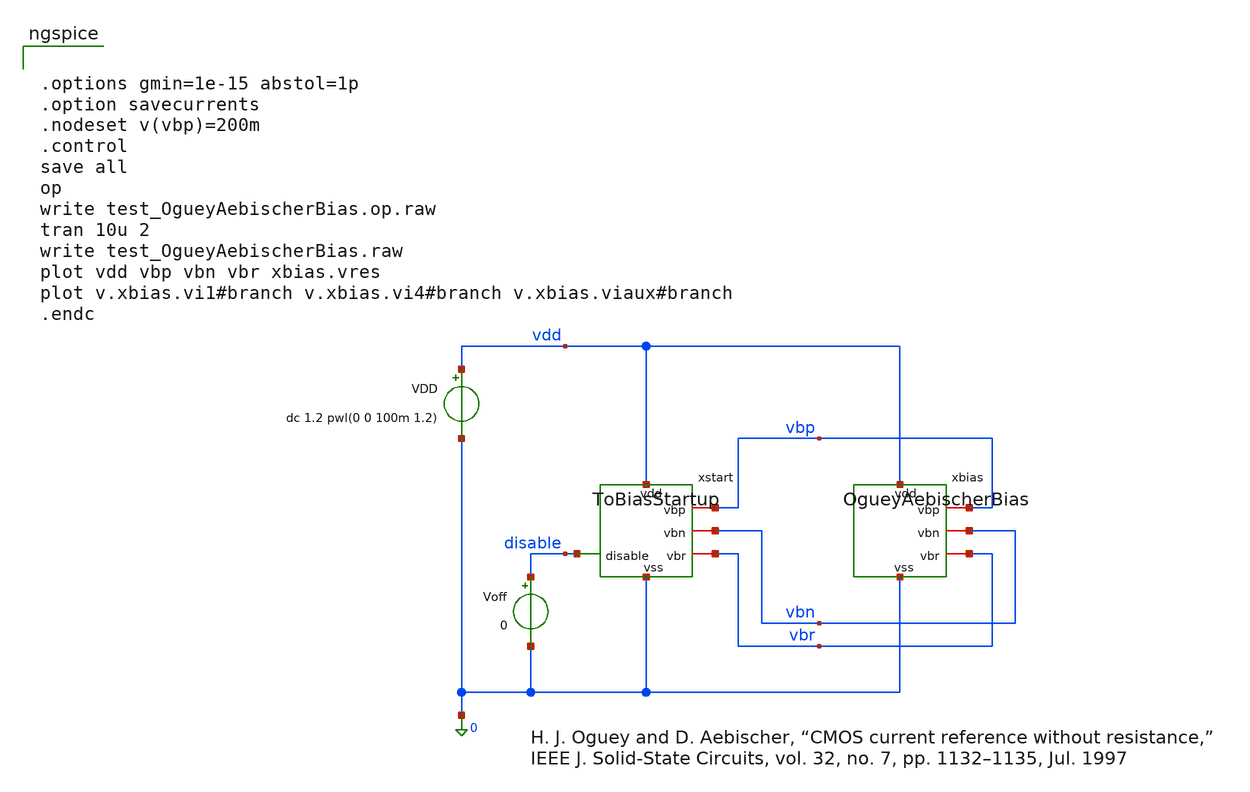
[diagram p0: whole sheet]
** sch_path: playground/test_OgueyAebischerBias.sch
**.subckt test_OgueyAebischerBias
xbias vdd vbp vbn vbr 0 OgueyAebischerBias
xstart vdd vbp vbn disable vbr 0 ToBiasStartup
VDD vdd 0 dc 1.2 pwl(0 0 100m 1.2)
Voff disable 0 0
**** begin user architecture code


.options gmin=1e-15 abstol=1p
.option savecurrents
.nodeset v(vbp)=200m
.control
save all
op
write test_OgueyAebischerBias.op.raw
tran 10u 2
write test_OgueyAebischerBias.raw
plot vdd vbp vbn vbr xbias.vres
plot v.xbias.vi1#branch v.xbias.vi4#branch v.xbias.viaux#branch
.endc


 .lib $::SKYWATER_MODELS/models/sky130.lib.spice tt

.param mc_mm_switch=0
.param mc_pr_switch=1


**** end user architecture code
**.ends

* expanding   symbol:  OgueyAebischerBias.sym # of pins=5
** sym_path: OgueyAebischerBias.sym
** sch_path: OgueyAebischerBias.sch
.subckt OgueyAebischerBias vdd vbp vbn vbr vss
*.iopin vss
*.iopin vdd
*.iopin vbp
*.iopin vbn
*.iopin vbr
XM10 net3 vbn vres vss sky130_fd_pr__nfet_01v8 L=1 W=1 nf=1 ad='int((1 + 1)/2) * 1 / 1 * 0.29' as='int((1 + 2)/2) * 1 / 1 * 0.29'
+ pd='2*int((1 + 1)/2) * (1 / 1 + 0.29)' ps='2*int((1 + 2)/2) * (1 / 1 + 0.29)' nrd='0.29 / 1 ' nrs='0.29 / 1 '
+ sa=0 sb=0 sd=0 mult=4 m=4
XM12 vbp vbp vdd vdd sky130_fd_pr__pfet_01v8 L=1 W=1 nf=1 ad='int((nf+1)/2) * W/nf * 0.29' as='int((nf+2)/2) * W/nf * 0.29'
+ pd='2*int((nf+1)/2) * (W/nf + 0.29)' ps='2*int((nf+2)/2) * (W/nf + 0.29)' nrd='0.29 / W' nrs='0.29 / W'
+ sa=0 sb=0 sd=0 mult=1 m=1
XM11 vbn vbn vss vss sky130_fd_pr__nfet_01v8 L=1 W=1 nf=1 ad='int((1 + 1)/2) * 1 / 1 * 0.29' as='int((1 + 2)/2) * 1 / 1 * 0.29'
+ pd='2*int((1 + 1)/2) * (1 / 1 + 0.29)' ps='2*int((1 + 2)/2) * (1 / 1 + 0.29)' nrd='0.29 / 1 ' nrs='0.29 / 1 '
+ sa=0 sb=0 sd=0 mult=1 m=1
XM13 net2 vbp vdd vdd sky130_fd_pr__pfet_01v8 L=1 W=1 nf=1 ad='int((nf+1)/2) * W/nf * 0.29' as='int((nf+2)/2) * W/nf * 0.29'
+ pd='2*int((nf+1)/2) * (W/nf + 0.29)' ps='2*int((nf+2)/2) * (W/nf + 0.29)' nrd='0.29 / W' nrs='0.29 / W'
+ sa=0 sb=0 sd=0 mult=4 m=4
XM14 net1 vbp vdd vdd sky130_fd_pr__pfet_01v8 L=1 W=1 nf=1 ad='int((nf+1)/2) * W/nf * 0.29' as='int((nf+2)/2) * W/nf * 0.29'
+ pd='2*int((nf+1)/2) * (W/nf + 0.29)' ps='2*int((nf+2)/2) * (W/nf + 0.29)' nrd='0.29 / W' nrs='0.29 / W'
+ sa=0 sb=0 sd=0 mult=2 m=2
XM16 vres vbr vss vss sky130_fd_pr__nfet_01v8 L=80 W=1 nf=1 ad='int((1 + 1)/2) * 1 / 1 * 0.29' as='int((1 + 2)/2) * 1 / 1 * 0.29'
+ pd='2*int((1 + 1)/2) * (1 / 1 + 0.29)' ps='2*int((1 + 2)/2) * (1 / 1 + 0.29)' nrd='0.29 / 1 ' nrs='0.29 / 1 '
+ sa=0 sb=0 sd=0 mult=1 m=1
XM15 vbr vbr vss vss sky130_fd_pr__nfet_01v8 L=80 W=1 nf=1 ad='int((1 + 1)/2) * 1 / 1 * 0.29' as='int((1 + 2)/2) * 1 / 1 * 0.29'
+ pd='2*int((1 + 1)/2) * (1 / 1 + 0.29)' ps='2*int((1 + 2)/2) * (1 / 1 + 0.29)' nrd='0.29 / 1 ' nrs='0.29 / 1 '
+ sa=0 sb=0 sd=0 mult=1 m=1
Vi1 vbp net3 0
.save i(vi1)
Vi4 net2 vbn 0
.save i(vi4)
Viaux net1 vbr 0
.save i(viaux)
.ends


* expanding   symbol:  ToBiasStartup.sym # of pins=6
** sym_path: ToBiasStartup.sym
** sch_path: ToBiasStartup.sch
.subckt ToBiasStartup vdd vbp vbn disable vbr vss
*.iopin vss
*.iopin vdd
*.iopin vbp
*.iopin vbn
*.iopin vbr
*.ipin disable
XM24 vbr disable vss vss sky130_fd_pr__nfet_01v8 L=0.3 W=1 nf=1 ad='int((1 + 1)/2) * 1 / 1 * 0.29' as='int((1 + 2)/2) * 1 / 1 * 0.29'
+ pd='2*int((1 + 1)/2) * (1 / 1 + 0.29)' ps='2*int((1 + 2)/2) * (1 / 1 + 0.29)' nrd='0.29 / 1 ' nrs='0.29 / 1 '
+ sa=0 sb=0 sd=0 mult=1 m=1
XM22 vbr vkick vdd vdd sky130_fd_pr__pfet_01v8 L=0.3 W=1 nf=1 ad='int((nf+1)/2) * W/nf * 0.29' as='int((nf+2)/2) * W/nf * 0.29'
+ pd='2*int((nf+1)/2) * (W/nf + 0.29)' ps='2*int((nf+2)/2) * (W/nf + 0.29)' nrd='0.29 / W' nrs='0.29 / W'
+ sa=0 sb=0 sd=0 mult=1 m=1
XM25 vkick vbp vdd vdd sky130_fd_pr__pfet_01v8 L=0.3 W=1 nf=1 ad='int((nf+1)/2) * W/nf * 0.29' as='int((nf+2)/2) * W/nf * 0.29'
+ pd='2*int((nf+1)/2) * (W/nf + 0.29)' ps='2*int((nf+2)/2) * (W/nf + 0.29)' nrd='0.29 / W' nrs='0.29 / W'
+ sa=0 sb=0 sd=0 mult=1 m=1
XM23 vbn disable vss vss sky130_fd_pr__nfet_01v8 L=0.3 W=1 nf=1 ad='int((1 + 1)/2) * 1 / 1 * 0.29' as='int((1 + 2)/2) * 1 / 1 * 0.29'
+ pd='2*int((1 + 1)/2) * (1 / 1 + 0.29)' ps='2*int((1 + 2)/2) * (1 / 1 + 0.29)' nrd='0.29 / 1 ' nrs='0.29 / 1 '
+ sa=0 sb=0 sd=0 mult=1 m=1
XM21 vbn vkick vdd vdd sky130_fd_pr__pfet_01v8 L=0.3 W=1 nf=1 ad='int((nf+1)/2) * W/nf * 0.29' as='int((nf+2)/2) * W/nf * 0.29'
+ pd='2*int((nf+1)/2) * (W/nf + 0.29)' ps='2*int((nf+2)/2) * (W/nf + 0.29)' nrd='0.29 / W' nrs='0.29 / W'
+ sa=0 sb=0 sd=0 mult=1 m=1
XM20 disable vkick disable vss sky130_fd_pr__nfet_01v8 L=40 W=40 nf=1 ad='int((1 + 1)/2) * 40 / 1 * 0.29'
+ as='int((1 + 2)/2) * 40 / 1 * 0.29' pd='2*int((1 + 1)/2) * (40 / 1 + 0.29)' ps='2*int((1 + 2)/2) * (40 / 1 + 0.29)'
+ nrd='0.29 / 40 ' nrs='0.29 / 40 ' sa=0 sb=0 sd=0 mult=1 m=1
XM26 vdd vbp vdd vss sky130_fd_pr__nfet_01v8 L=40 W=40 nf=1 ad='int((1 + 1)/2) * 40 / 1 * 0.29' as='int((1 + 2)/2) * 40 / 1 * 0.29'
+ pd='2*int((1 + 1)/2) * (40 / 1 + 0.29)' ps='2*int((1 + 2)/2) * (40 / 1 + 0.29)' nrd='0.29 / 40 ' nrs='0.29 / 40 '
+ sa=0 sb=0 sd=0 mult=1 m=1
.ends

.end
